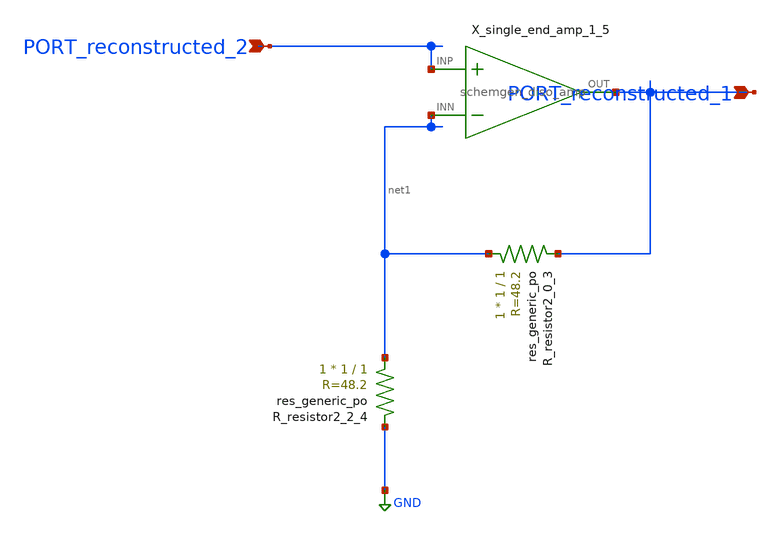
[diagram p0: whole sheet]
** sch_path: schematics/Image2Net/096.sch
**.subckt 096 PORT_reconstructed_1 PORT_reconstructed_2
*.ipin PORT_reconstructed_1
*.ipin PORT_reconstructed_2
XR_resistor2_0_3 net1 PORT_reconstructed_1 sky130_fd_pr__res_generic_po W=1 L=1 m=1
XR_resistor2_2_4 net1 GND sky130_fd_pr__res_generic_po W=1 L=1 m=1
X_single_end_amp_1_5 PORT_reconstructed_2 net1 PORT_reconstructed_1 schemgen_diso_amp
**.ends

* expanding   symbol:  schemgen_diso_amp.sym # of pins=3
** sym_path: symbols/schemgen_diso_amp.sym
.subckt schemgen_diso_amp INP INN OUT
* SchemGen ideal op-amp: Vout = 1e5 * (V(INP) - V(INN))
E1 OUT 0 INP INN 1e5
.ends schemgen_diso_amp
.GLOBAL GND
.end
